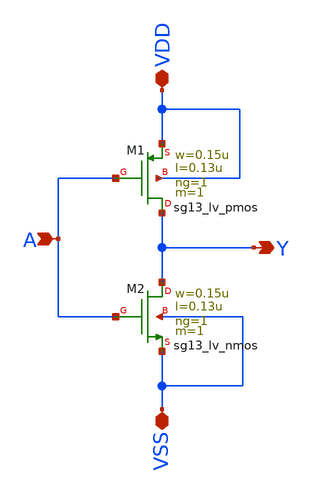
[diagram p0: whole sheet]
** sch_path: Inverter3.sch
**.subckt Inverter3 A VSS VDD Y
*.ipin A
*.iopin VSS
*.iopin VDD
*.opin Y
XM2 Y A VSS VSS sg13_lv_nmos w=0.15u l=0.13u ng=1 m=1 mm_ok=1
XM1 Y A VDD VDD sg13_lv_pmos w=0.15u l=0.13u ng=1 m=1 mm_ok=1
**.ends
.end
